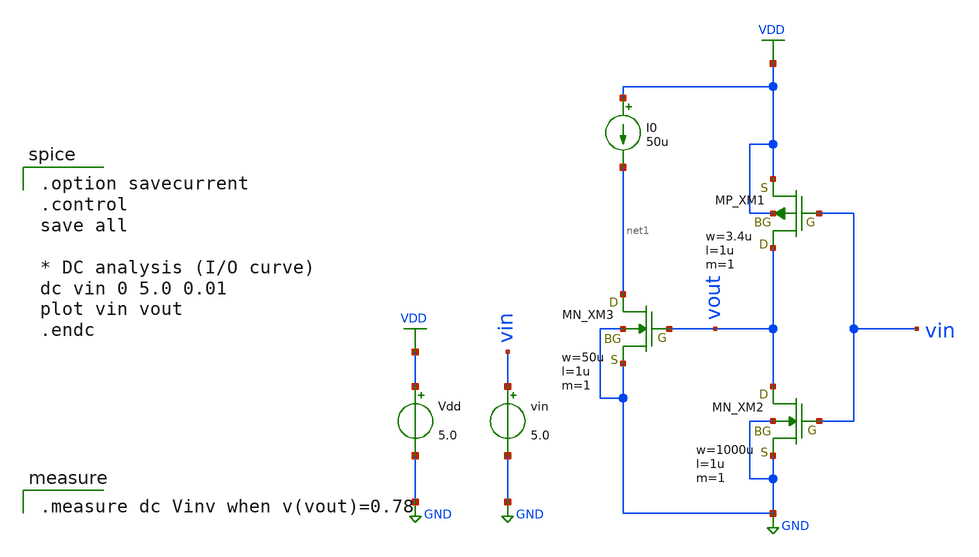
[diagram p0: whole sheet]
** sch_path: schematic/20250924_OSS_Workshop/ishikai/CS/cs_startup_tb.sch
**.subckt cs_startup_tb
Vdd VDD GND 5.0
vin vin GND 5.0
I0 VDD net1 50u
XM1 vout vin VDD VDD PMOS w=3.4u l=1u as=0 ad=0 ps=0 pd=0 nrd=0 nrs=0 m=1
XM2 vout vin GND GND NMOS w=1000u l=1u as=0 ad=0 ps=0 pd=0 nrd=0 nrs=0 m=1
XM3 net1 vout GND GND NMOS w=50u l=1u as=0 ad=0 ps=0 pd=0 nrd=0 nrs=0 m=1
**** begin user architecture code

.option savecurrent
.control
save all

* DC analysis (I/O curve)
dc vin 0 5.0 0.01
plot vin vout
.endc


.measure dc Vinv when v(vout)=0.78

 .include $::LIB/../ip62_models
**** end user architecture code
**.ends
.GLOBAL VDD
.GLOBAL GND
.end
